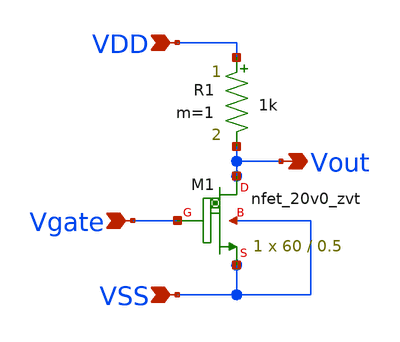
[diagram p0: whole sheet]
** sch_path: design/THESIS_EXP_RO_INVERTER_SKY130A/INV_ZVT_R.sch
**.subckt INV_ZVT_R VDD VSS Vgate Vout
*.ipin VDD
*.ipin VSS
*.ipin Vgate
*.opin Vout
R1 VDD Vout 1k m=1
XM1 Vout Vgate VSS VSS sky130_fd_pr__nfet_20v0_zvt W=60 L=0.5 m=1
**.ends
.end
